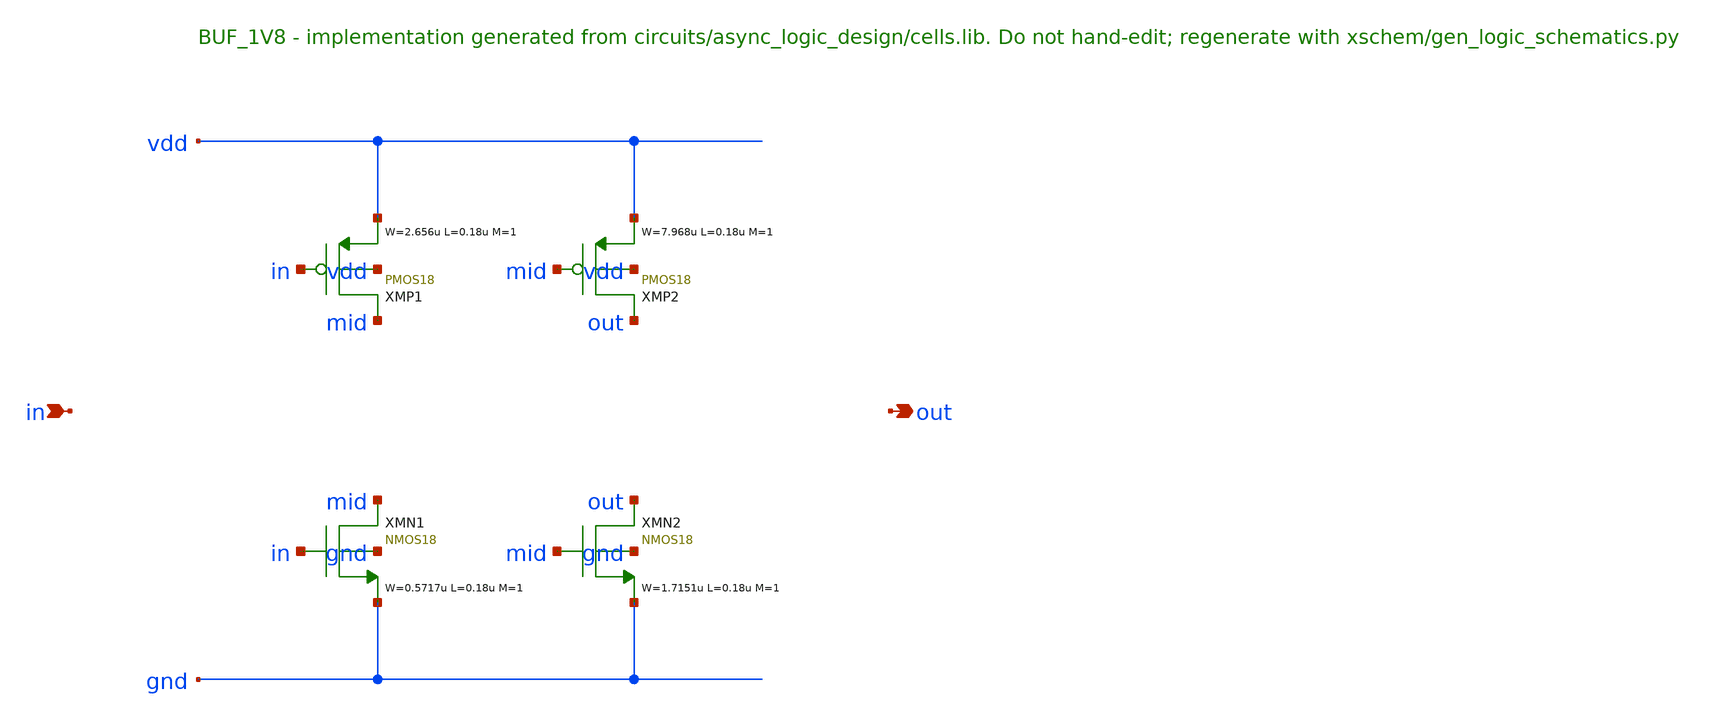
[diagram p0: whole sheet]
** sch_path: xschem/logic/BUF_1V8.sch
**.subckt BUF_1V8 in out
*.ipin in
*.opin out
XMP1 mid in vdd vdd PMOS18 W=2.656u L=0.18u M=1 MM_SIGMA=0
XMP2 out mid vdd vdd PMOS18 W=7.968u L=0.18u M=1 MM_SIGMA=0
XMN1 mid in gnd gnd NMOS18 W=0.5717u L=0.18u M=1 MM_SIGMA=0
XMN2 out mid gnd gnd NMOS18 W=1.7151u L=0.18u M=1 MM_SIGMA=0
**.ends
.end
